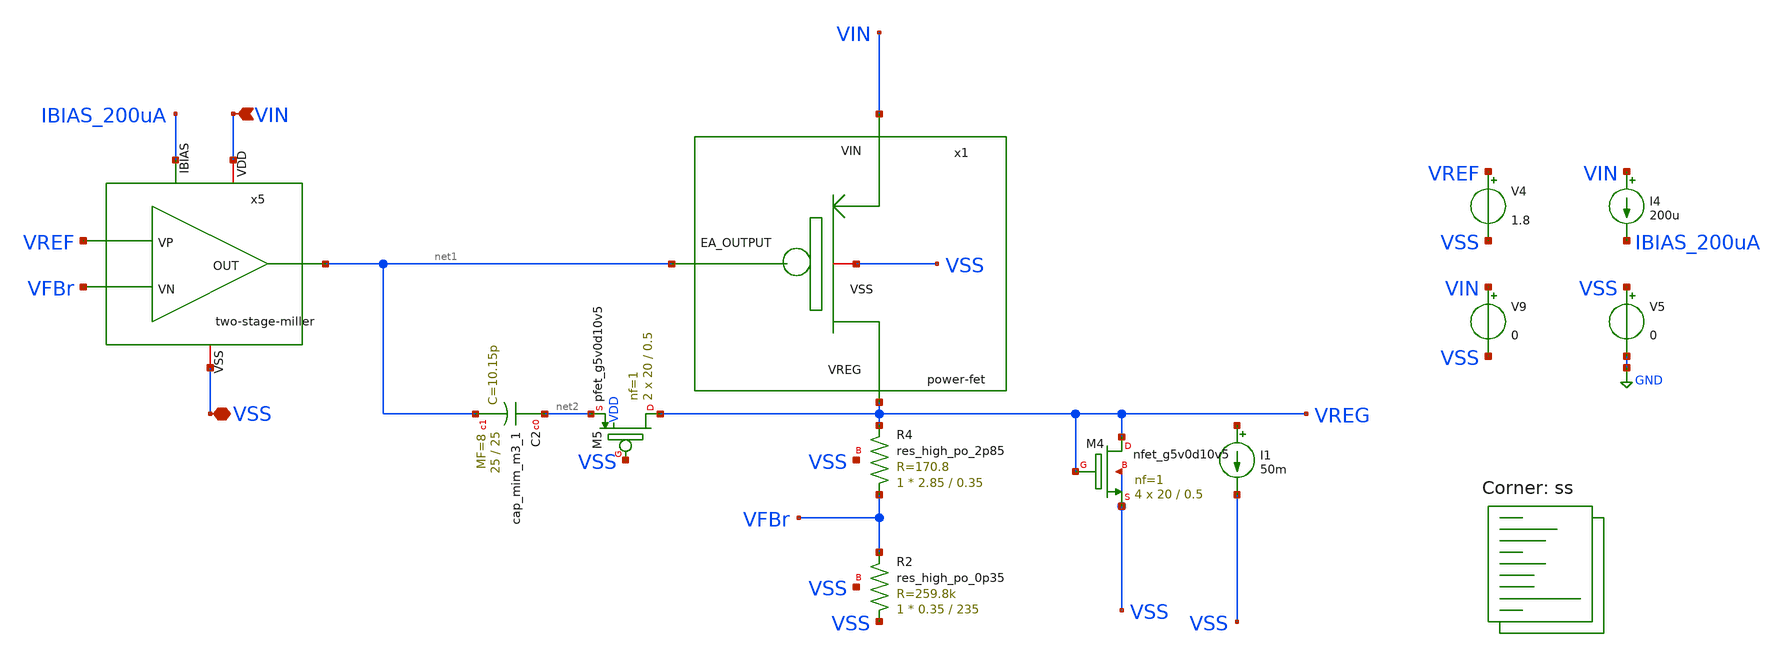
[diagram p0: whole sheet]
** sch_path: bandgap/testbench/tb_dc_dropout.sch
**.subckt tb_dc_dropout VIN VSS
*.ipin VIN
*.iopin VSS
V4 VREF VSS 1.8
V5 VSS GND 0
V9 VIN VSS 0
x1 VIN VSS net1 VREG power-fet
XR2 VSS VFBr VSS sky130_fd_pr__res_high_po_0p35 L=235 mult=1 m=1
XR4 VFBr VREG VSS sky130_fd_pr__res_high_po_2p85 L=0.35 mult=1 m=1
x5 VIN net1 VREF VFBr IBIAS_200uA VSS two-stage-miller
XM4 VREG VREG VSS VSS sky130_fd_pr__nfet_g5v0d10v5 L=0.5 W=20 nf=1 ad='int((nf+1)/2) * W/nf * 0.29' as='int((nf+2)/2) * W/nf * 0.29'
+ pd='2*int((nf+1)/2) * (W/nf + 0.29)' ps='2*int((nf+2)/2) * (W/nf + 0.29)' nrd='0.29 / W' nrs='0.29 / W'
+ sa=0 sb=0 sd=0 mult=4 m=4
XC2 net2 net1 sky130_fd_pr__cap_mim_m3_1 W=25 L=25 MF=8 m=8
XM5 VREG VSS net2 VDD sky130_fd_pr__pfet_g5v0d10v5 L=0.5 W=20 nf=1 ad='int((nf+1)/2) * W/nf * 0.29' as='int((nf+2)/2) * W/nf * 0.29'
+ pd='2*int((nf+1)/2) * (W/nf + 0.29)' ps='2*int((nf+2)/2) * (W/nf + 0.29)' nrd='0.29 / W' nrs='0.29 / W'
+ sa=0 sb=0 sd=0 mult=2 m=2
I1 net3 VSS 50m
I4 VIN IBIAS_200uA 200u
**** begin user architecture code


.control
DC V9 0 10.5 0.01

* Nominal output voltage (from regulation region)
let Vout_nom = 1.25
let Vout_95  = 0.95*Vout_nom

* Find Vin where Vout crosses 95%
meas dc Vin_do find v(vin) when v(vreg)=Vout_95

* Measure Vout at that Vin (for completeness)
meas dc Vout_do find v(vreg) when v(vreg)=Vout_95

* Compute dropout voltage
let Vdo = Vin_do - Vout_do
print vdo
plot VIN VREG
.endc


.lib $::SKYWATER_MODELS/sky130.lib.spice ss
**** end user architecture code
**.ends
.GLOBAL GND
.end
